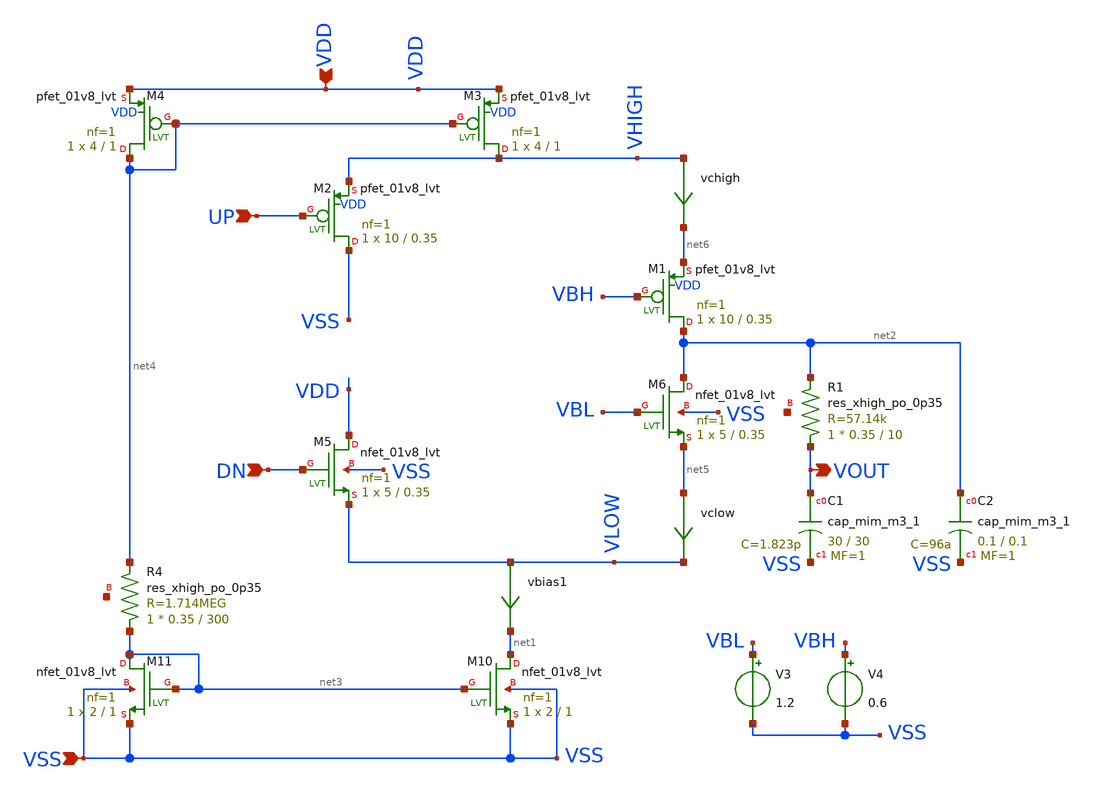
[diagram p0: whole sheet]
** sch_path: xschem/pll_cp_alpha.sch
**.subckt pll_cp_alpha UP VOUT DN VDD VSS
*.ipin UP
*.opin VOUT
*.ipin DN
*.ipin VDD
*.ipin VSS
XM5 VDD DN VLOW VSS sky130_fd_pr__nfet_01v8_lvt L=0.35 W=5 nf=1 ad='int((nf+1)/2) * W/nf * 0.29' as='int((nf+2)/2) * W/nf * 0.29'
+ pd='2*int((nf+1)/2) * (W/nf + 0.29)' ps='2*int((nf+2)/2) * (W/nf + 0.29)' nrd='0.29 / W' nrs='0.29 / W'
+ sa=0 sb=0 sd=0 mult=1 m=1
XM6 net2 VBL net5 VSS sky130_fd_pr__nfet_01v8_lvt L=0.35 W=5 nf=1 ad='int((nf+1)/2) * W/nf * 0.29' as='int((nf+2)/2) * W/nf * 0.29'
+ pd='2*int((nf+1)/2) * (W/nf + 0.29)' ps='2*int((nf+2)/2) * (W/nf + 0.29)' nrd='0.29 / W' nrs='0.29 / W'
+ sa=0 sb=0 sd=0 mult=1 m=1
XM10 net1 net3 VSS VSS sky130_fd_pr__nfet_01v8_lvt L=1 W=2 nf=1 ad='int((nf+1)/2) * W/nf * 0.29' as='int((nf+2)/2) * W/nf * 0.29'
+ pd='2*int((nf+1)/2) * (W/nf + 0.29)' ps='2*int((nf+2)/2) * (W/nf + 0.29)' nrd='0.29 / W' nrs='0.29 / W'
+ sa=0 sb=0 sd=0 mult=1 m=1
vbias1 VLOW net1 0
.save i(vbias1)
XM1 net2 VBH net6 VDD sky130_fd_pr__pfet_01v8_lvt L=0.35 W=10 nf=1 ad='int((nf+1)/2) * W/nf * 0.29' as='int((nf+2)/2) * W/nf * 0.29'
+ pd='2*int((nf+1)/2) * (W/nf + 0.29)' ps='2*int((nf+2)/2) * (W/nf + 0.29)' nrd='0.29 / W' nrs='0.29 / W'
+ sa=0 sb=0 sd=0 mult=1 m=1
XM2 VSS UP VHIGH VDD sky130_fd_pr__pfet_01v8_lvt L=0.35 W=10 nf=1 ad='int((nf+1)/2) * W/nf * 0.29' as='int((nf+2)/2) * W/nf * 0.29'
+ pd='2*int((nf+1)/2) * (W/nf + 0.29)' ps='2*int((nf+2)/2) * (W/nf + 0.29)' nrd='0.29 / W' nrs='0.29 / W'
+ sa=0 sb=0 sd=0 mult=1 m=1
XC1 VOUT VSS sky130_fd_pr__cap_mim_m3_1 W=30 L=30 MF=1 m=1
XM11 net3 net3 VSS VSS sky130_fd_pr__nfet_01v8_lvt L=1 W=2 nf=1 ad='int((nf+1)/2) * W/nf * 0.29' as='int((nf+2)/2) * W/nf * 0.29'
+ pd='2*int((nf+1)/2) * (W/nf + 0.29)' ps='2*int((nf+2)/2) * (W/nf + 0.29)' nrd='0.29 / W' nrs='0.29 / W'
+ sa=0 sb=0 sd=0 mult=1 m=1
XR4 net3 net4 net7 sky130_fd_pr__res_xhigh_po_0p35 L=300 mult=1 m=1
XM3 VHIGH net4 VDD VDD sky130_fd_pr__pfet_01v8_lvt L=1 W=4 nf=1 ad='int((nf+1)/2) * W/nf * 0.29' as='int((nf+2)/2) * W/nf * 0.29'
+ pd='2*int((nf+1)/2) * (W/nf + 0.29)' ps='2*int((nf+2)/2) * (W/nf + 0.29)' nrd='0.29 / W' nrs='0.29 / W'
+ sa=0 sb=0 sd=0 mult=1 m=1
XM4 net4 net4 VDD VDD sky130_fd_pr__pfet_01v8_lvt L=1 W=4 nf=1 ad='int((nf+1)/2) * W/nf * 0.29' as='int((nf+2)/2) * W/nf * 0.29'
+ pd='2*int((nf+1)/2) * (W/nf + 0.29)' ps='2*int((nf+2)/2) * (W/nf + 0.29)' nrd='0.29 / W' nrs='0.29 / W'
+ sa=0 sb=0 sd=0 mult=1 m=1
V3 VBL VSS 1.2
vclow net5 VLOW 0
.save i(vclow)
vchigh VHIGH net6 0
.save i(vchigh)
V4 VBH VSS 0.6
XR1 VOUT net2 net8 sky130_fd_pr__res_xhigh_po_0p35 L=10 mult=1 m=1
XC2 net2 VSS sky130_fd_pr__cap_mim_m3_1 W=0.1 L=0.1 MF=1 m=1
**.ends
.end
